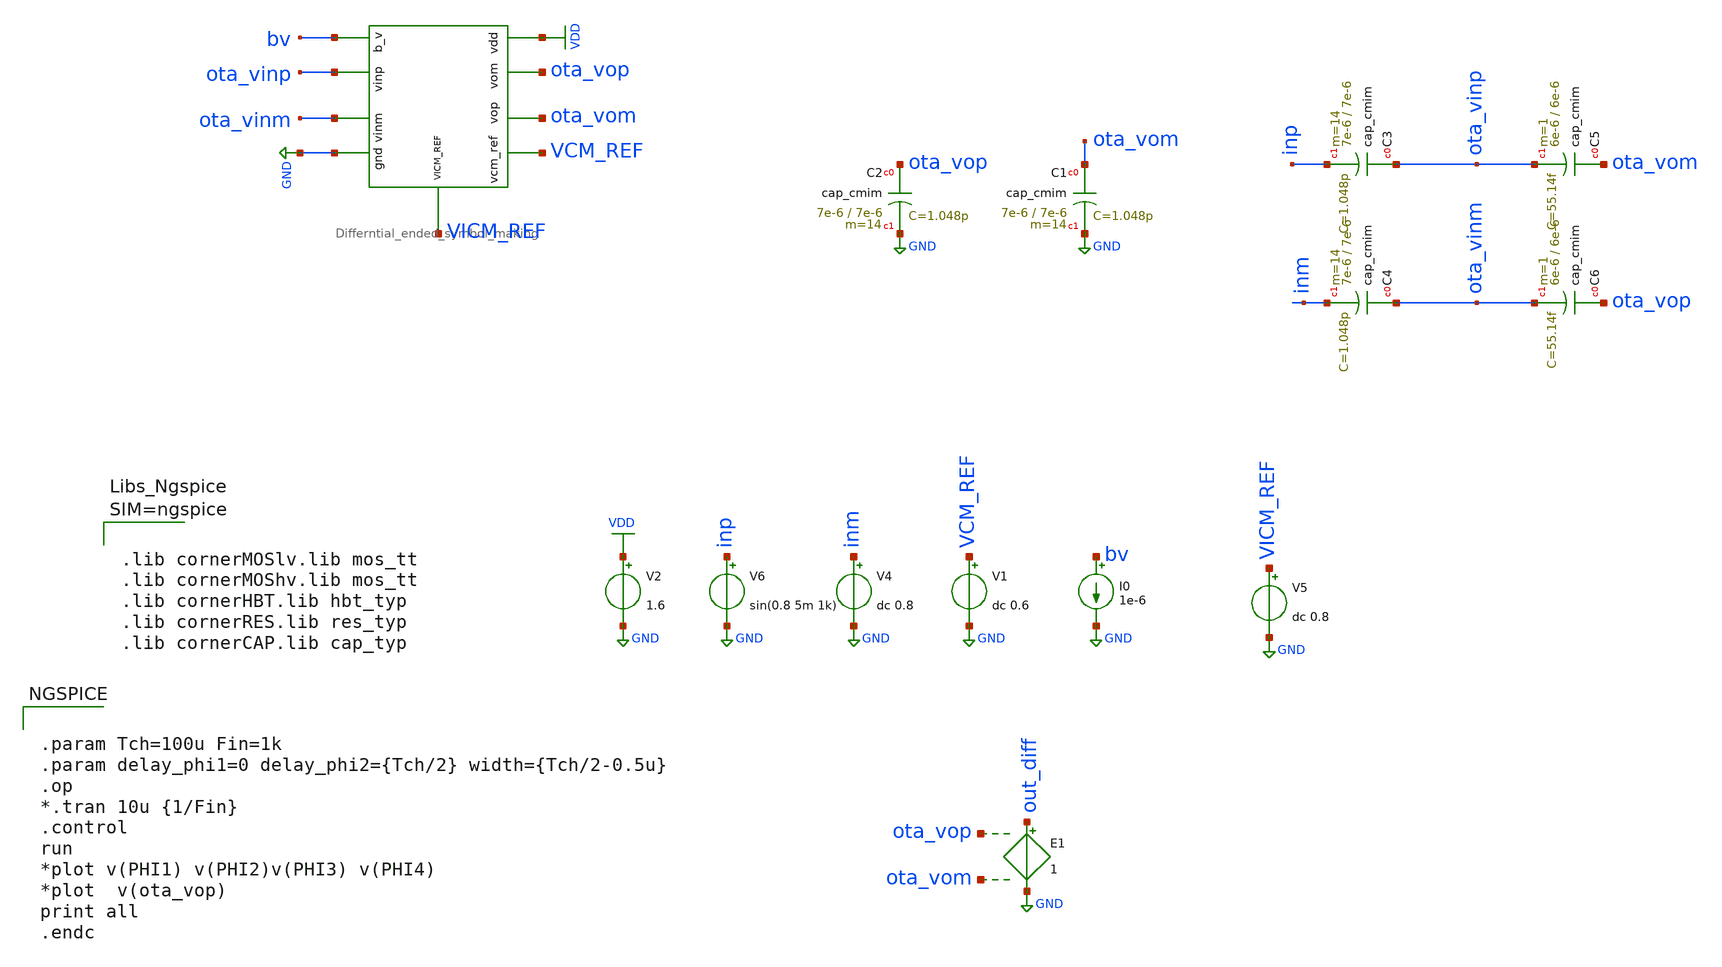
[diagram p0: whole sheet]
** sch_path: tb_ota.sch
**.subckt tb_ota
V2 VDD GND 1.6
V4 inm GND dc 0.8
V1 VCM_REF GND dc 0.6
I0 bv GND 1e-6
x2 VDD VCM_REF ota_vop ota_vom GND bv ota_vinm ota_vinp VICM_REF Differntial_ended_symbol_making
V5 VICM_REF GND dc 0.8
XC1 ota_vom GND cap_cmim w=7e-6 l=7e-6 m=14 mm_ok=1
XC2 ota_vop GND cap_cmim w=7e-6 l=7e-6 m=14 mm_ok=1
E1 out_diff GND ota_vop ota_vom 1
XC3 ota_vinp inp cap_cmim w=7e-6 l=7e-6 m=14 mm_ok=1
XC4 ota_vinm inm cap_cmim w=7e-6 l=7e-6 m=14 mm_ok=1
XC5 ota_vom ota_vinp cap_cmim w=6e-6 l=6e-6 m=1 mm_ok=1
XC6 ota_vop ota_vinm cap_cmim w=6e-6 l=6e-6 m=1 mm_ok=1
V6 inp GND sin(0.8 5m 1k)
**** begin user architecture code



.lib cornerMOSlv.lib mos_tt
.lib cornerMOShv.lib mos_tt
.lib cornerHBT.lib hbt_typ
.lib cornerRES.lib res_typ
.lib cornerCAP.lib cap_typ





.param Tch=100u Fin=1k
.param delay_phi1=0 delay_phi2={Tch/2} width={Tch/2-0.5u}
.op
*.tran 10u {1/Fin}
.control
run
*plot v(PHI1) v(PHI2)v(PHI3) v(PHI4)
*plot  v(ota_vop)
print all
.endc


**** end user architecture code
**.ends

* expanding   symbol:
*+  /home/prabhas/unic-cass-example/UNI-CASS_Project/final_Design_file/Differntial_ended_symbol_making.sym # of pins=9
** sym_path: Differntial_ended_symbol_making.sym
** sch_path: Differntial_ended_symbol_making.sch
.subckt Differntial_ended_symbol_making vdd vcm_ref vom vop gnd b_v vinm vinp VICM_REF
*.iopin b_v
*.iopin vinm
*.iopin vcm_ref
*.iopin vinp
*.iopin vop
*.iopin vom
*.iopin gnd
*.iopin vdd
*.iopin VICM_REF
XM7 vop nbias gnd gnd sg13_hv_nmos w=2u l=2u ng=1 m=2 mm_ok=1
XM8 vop vinm tail vdd sg13_hv_pmos w=4.5u l=1u ng=1 m=2 mm_ok=1
XM9 vom nbias gnd gnd sg13_hv_nmos w=2u l=2u ng=1 m=2 mm_ok=1
XM10 vom vinp tail vdd sg13_hv_pmos w=4.5u l=1u ng=1 m=2 mm_ok=1
XM11 tail b_v vdd vdd sg13_hv_pmos w=4u l=1u ng=1 m=4 mm_ok=1
XM6 net1 net1 gnd gnd sg13_hv_nmos w=1u l=0.5u ng=1 m=1 mm_ok=1
XM13 net1 vop tail_cmfb vdd sg13_hv_pmos w=2.25u l=0.50u ng=1 m=1 mm_ok=1
XM14 nbias net1 gnd gnd sg13_hv_nmos w=1u l=0.5u ng=1 m=1 mm_ok=1
XM15 nbias vcm_ref tail_cmfb vdd sg13_hv_pmos w=2.25u l=0.5u ng=1 m=2 mm_ok=1
XM16 tail_cmfb b_v vdd vdd sg13_hv_pmos w=4u l=1u ng=1 m=4 mm_ok=1
XM17 net1 vom tail_cmfb vdd sg13_hv_pmos w=2.25u l=0.50u ng=1 m=1 mm_ok=1
XM1 b_v b_v vdd vdd sg13_hv_pmos w=4u l=1u ng=1 m=1 mm_ok=1
XC1 nbias gnd cap_cmim w=14.0e-6 l=50.0e-6 m=1 mm_ok=1
XM2 VICM_REF vinm vinm vdd sg13_hv_pmos w=50u l=1u ng=5 m=1 mm_ok=1
XM3 VICM_REF vinp vinp vdd sg13_hv_pmos w=50u l=1u ng=5 m=1 mm_ok=1
XM4 vdd vdd vdd vdd sg13_hv_pmos w=4.5u l=0.4u ng=1 m=4 mm_ok=1
XM5 gnd gnd gnd gnd sg13_hv_nmos w=2u l=2u ng=1 m=4 mm_ok=1
.ends

.GLOBAL GND
.GLOBAL VDD
.end
